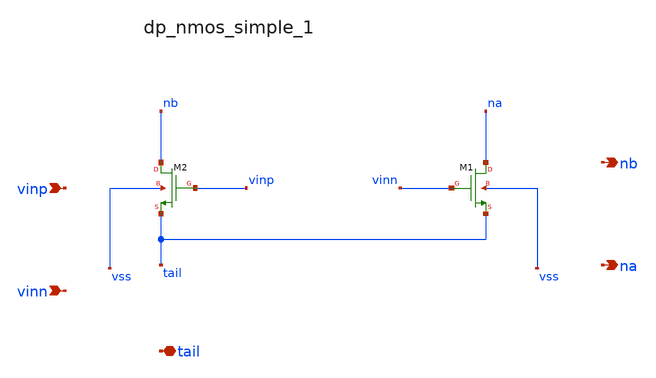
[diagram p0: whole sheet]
** sch_path: analog-db/raw/amp_033_ti_ldo_ref_selfbias/hier/blocks/dp_nmos_simple_1.sch
**.subckt dp_nmos_simple_1 vinp vinn tail nb na
*.ipin vinp
*.ipin vinn
*.iopin tail
*.opin nb
*.opin na
XM1 na vinn tail vss sg13_lv_nmos w=x_dut_xm1_w l=x_dut_xm1_l ng=1 m=1
XM2 nb vinp tail vss sg13_lv_nmos w=x_dut_xm2_w l=x_dut_xm2_l ng=1 m=1
**.ends
.end
